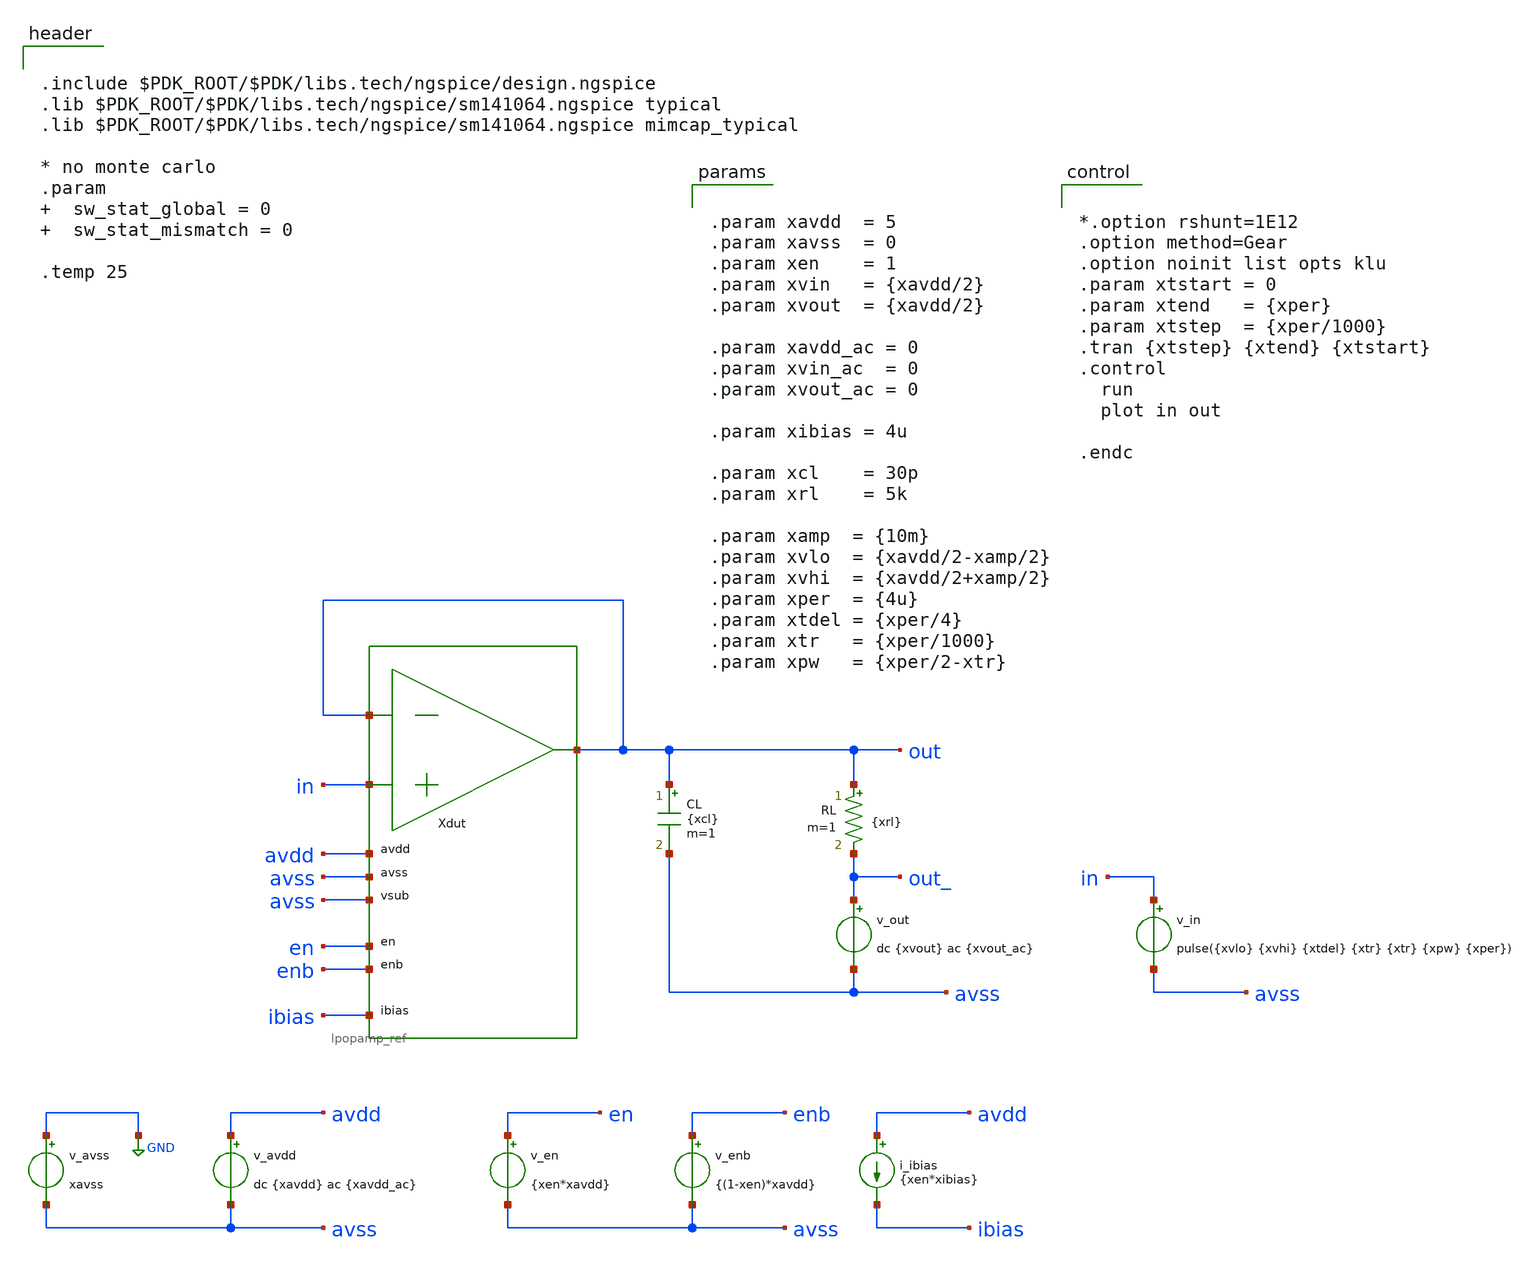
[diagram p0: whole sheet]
** sch_path: xschem/tb_lpopamp_buf_tran_step_small.sch
**.subckt tb_lpopamp_buf_tran_step_small
Xdut out in out avdd avss avss en enb ibias lpopamp_ref
v_avss GND avss xavss
v_avdd avdd avss dc {xavdd} ac {xavdd_ac}
v_in in avss pulse({xvlo} {xvhi} {xtdel} {xtr} {xtr} {xpw} {xper})
v_en en avss {xen*xavdd}
v_enb enb avss {(1-xen)*xavdd}
i_ibias avdd ibias {xen*xibias}
CL out avss {xcl} m=1
v_out out_ avss dc {xvout} ac {xvout_ac}
RL out out_ {xrl} m=1
**** begin user architecture code


.include $PDK_ROOT/$PDK/libs.tech/ngspice/design.ngspice
.lib $PDK_ROOT/$PDK/libs.tech/ngspice/sm141064.ngspice typical
.lib $PDK_ROOT/$PDK/libs.tech/ngspice/sm141064.ngspice mimcap_typical

* no monte carlo
.param   sw_stat_global = 0   sw_stat_mismatch = 0

.temp 25




*.option rshunt=1E12
.option method=Gear
.option noinit list opts klu
.param xtstart = 0
.param xtend   = {xper}
.param xtstep  = {xper/1000}
.tran {xtstep} {xtend} {xtstart}
.control
  run
  plot in out

.endc




.param xavdd  = 5
.param xavss  = 0
.param xen    = 1
.param xvin   = {xavdd/2}
.param xvout  = {xavdd/2}

.param xavdd_ac = 0
.param xvin_ac  = 0
.param xvout_ac = 0

.param xibias = 4u

.param xcl    = 30p
.param xrl    = 5k

.param xamp  = {10m}
.param xvlo  = {xavdd/2-xamp/2}
.param xvhi  = {xavdd/2+xamp/2}
.param xper  = {4u}
.param xtdel = {xper/4}
.param xtr   = {xper/1000}
.param xpw   = {xper/2-xtr}


**** end user architecture code
**.ends
.GLOBAL GND
.end
